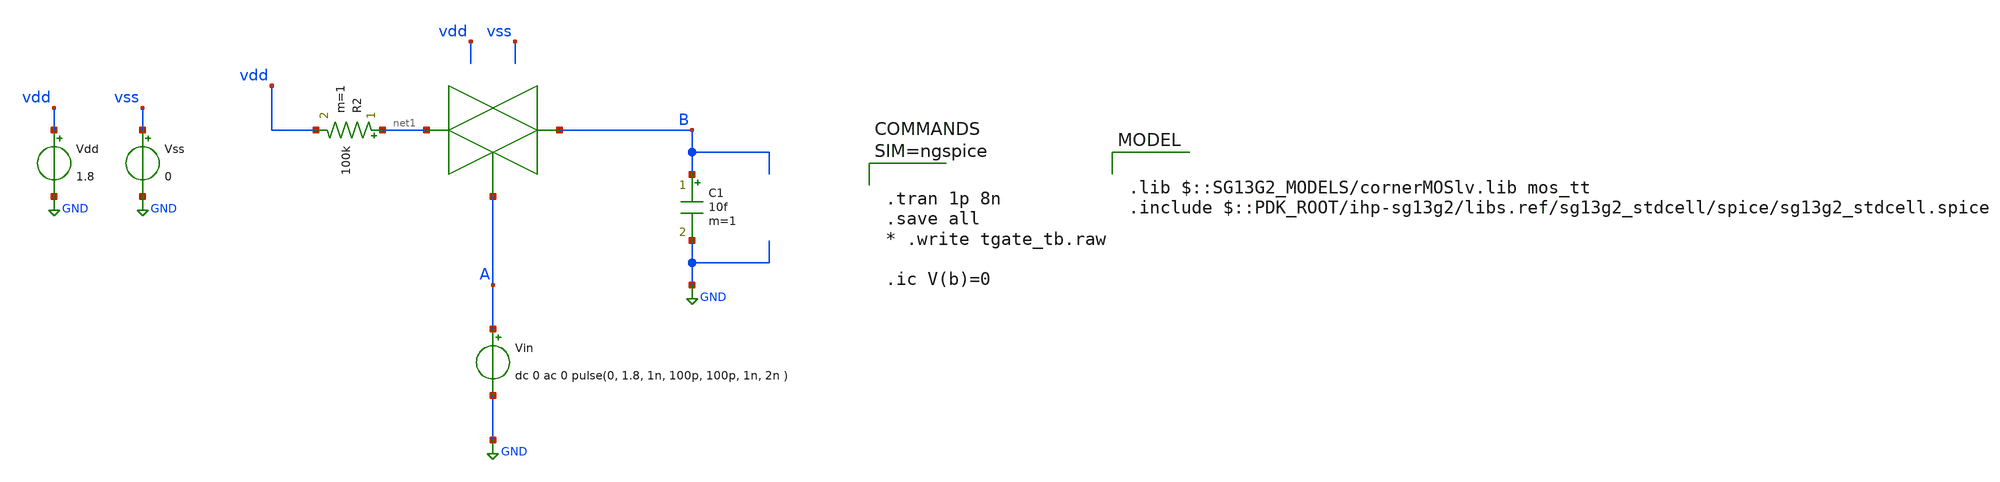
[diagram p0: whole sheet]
** sch_path: ngspice_cosim_tgate/tgate_tb.sch
**.subckt tgate_tb
Vin A GND dc 0 ac 0 pulse(0, 1.8, 1n, 100p, 100p, 1n, 2n )
Vdd vdd GND 1.8
Vss vss GND 0
R2 net1 vdd 100k m=1
C1 B GND 10f m=1
**** begin user architecture code



.tran 1p 8n
.save all
* .write tgate_tb.raw

.ic V(b)=0




.lib $::SG13G2_MODELS/cornerMOSlv.lib mos_tt
.include $::PDK_ROOT/ihp-sg13g2/libs.ref/sg13g2_stdcell/spice/sg13g2_stdcell.spice

**** end user architecture code
**.ends
.GLOBAL GND
.end
